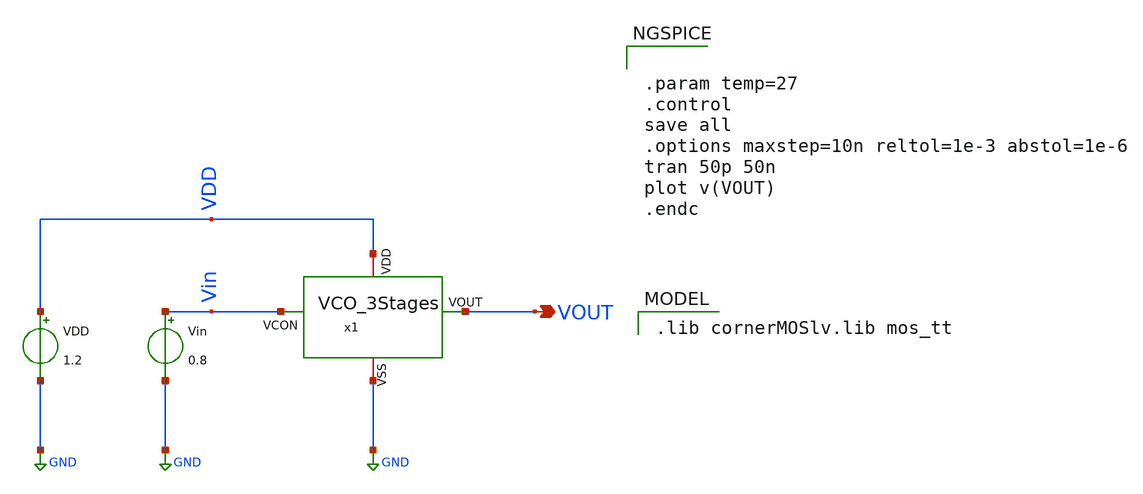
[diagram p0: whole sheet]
** sch_path: Team 1 Design/design_data/xschem/VCO/VCO_3Stages_tb.sch
**.subckt VCO_3Stages_tb VOUT
*.opin VOUT
VDD VDD GND 1.2
Vin Vin GND 0.8
x1 VDD VOUT Vin GND VCO_3Stages
**** begin user architecture code


.param temp=27
.control
save all
.options maxstep=10n reltol=1e-3 abstol=1e-6
tran 50p 50n
plot v(VOUT)
.endc


 .lib cornerMOSlv.lib mos_tt

**** end user architecture code
**.ends
.GLOBAL GND
.end
